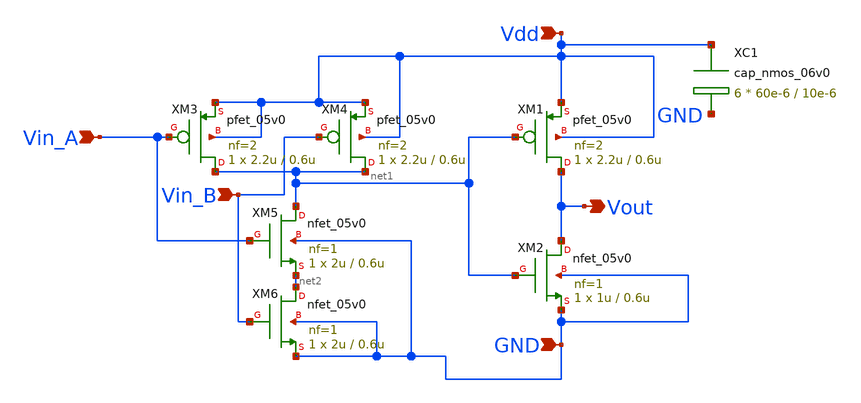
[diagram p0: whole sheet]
** sch_path: MG_decoder/MG_and_gate.sch
**.subckt MG_and_gate Vdd GND Vin_A Vout Vin_B
*.ipin Vdd
*.ipin GND
*.ipin Vin_A
*.opin Vout
*.ipin Vin_B
XM1 Vout net1 Vdd Vdd pfet_05v0 L=0.6u W=2.2u nf=2 ad='int((nf+1)/2) * W/nf * 0.18u' as='int((nf+2)/2) * W/nf * 0.18u'
+ pd='2*int((nf+1)/2) * (W/nf + 0.18u)' ps='2*int((nf+2)/2) * (W/nf + 0.18u)' nrd='0.18u / W' nrs='0.18u / W'
+ sa=0 sb=0 sd=0 m=1
XM2 Vout net1 GND GND nfet_05v0 L=0.6u W=1u nf=1 ad='int((nf+1)/2) * W/nf * 0.18u' as='int((nf+2)/2) * W/nf * 0.18u'
+ pd='2*int((nf+1)/2) * (W/nf + 0.18u)' ps='2*int((nf+2)/2) * (W/nf + 0.18u)' nrd='0.18u / W' nrs='0.18u / W'
+ sa=0 sb=0 sd=0 m=1
XM3 net1 Vin_A Vdd Vdd pfet_05v0 L=0.6u W=2.2u nf=2 ad='int((nf+1)/2) * W/nf * 0.18u' as='int((nf+2)/2) * W/nf * 0.18u'
+ pd='2*int((nf+1)/2) * (W/nf + 0.18u)' ps='2*int((nf+2)/2) * (W/nf + 0.18u)' nrd='0.18u / W' nrs='0.18u / W'
+ sa=0 sb=0 sd=0 m=1
XM4 net1 Vin_B Vdd Vdd pfet_05v0 L=0.6u W=2.2u nf=2 ad='int((nf+1)/2) * W/nf * 0.18u' as='int((nf+2)/2) * W/nf * 0.18u'
+ pd='2*int((nf+1)/2) * (W/nf + 0.18u)' ps='2*int((nf+2)/2) * (W/nf + 0.18u)' nrd='0.18u / W' nrs='0.18u / W'
+ sa=0 sb=0 sd=0 m=1
XM5 net1 Vin_A net2 GND nfet_05v0 L=0.6u W=2u nf=1 ad='int((nf+1)/2) * W/nf * 0.18u' as='int((nf+2)/2) * W/nf * 0.18u'
+ pd='2*int((nf+1)/2) * (W/nf + 0.18u)' ps='2*int((nf+2)/2) * (W/nf + 0.18u)' nrd='0.18u / W' nrs='0.18u / W'
+ sa=0 sb=0 sd=0 m=1
XM6 net2 Vin_B GND GND nfet_05v0 L=0.6u W=2u nf=1 ad='int((nf+1)/2) * W/nf * 0.18u' as='int((nf+2)/2) * W/nf * 0.18u'
+ pd='2*int((nf+1)/2) * (W/nf + 0.18u)' ps='2*int((nf+2)/2) * (W/nf + 0.18u)' nrd='0.18u / W' nrs='0.18u / W'
+ sa=0 sb=0 sd=0 m=1
XC1 Vdd GND cap_nmos_06v0 c_width=60e-6 c_length=10e-6 m=6
**.ends
.end
